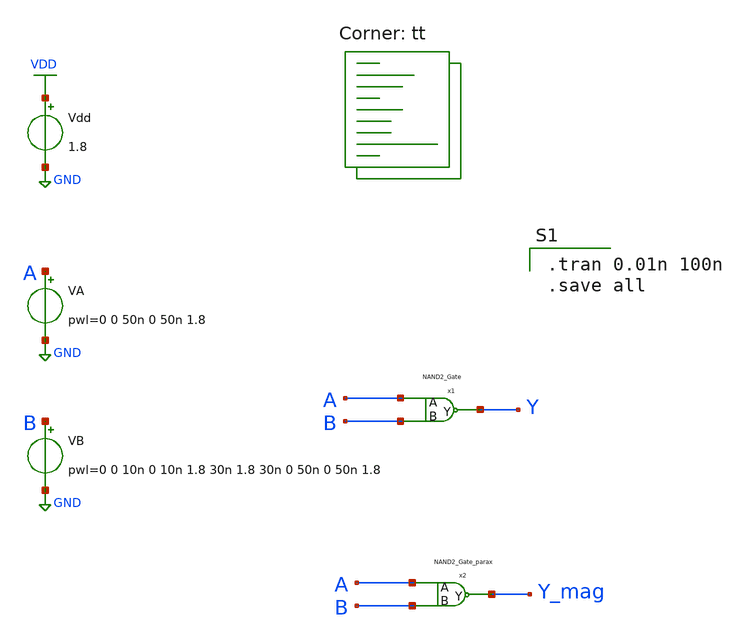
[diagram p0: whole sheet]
** sch_path: gates/NANN2sim.sch
**.subckt NANN2sim
Vdd VDD GND 1.8
VA A GND pwl=0 0 50n 0 50n 1.8
VB B GND pwl=0 0 10n 0 10n 1.8 30n 1.8 30n 0 50n 0 50n 1.8
x1 A Y B NAND2_Gate
x2 A Y_mag B NAND2_Gate_parax
**** begin user architecture code

.tran 0.01n 100n
.save all

.lib $::SKYWATER_MODELS/sky130.lib.spice tt
**** end user architecture code
**.ends

* expanding   symbol:  NAND2_Gate.sym # of pins=3
** sym_path: gates/NAND2_Gate.sym
** sch_path: gates/NAND2_Gate.sch
.subckt NAND2_Gate A Y B
*.ipin A
*.ipin B
*.opin Y
XM1 Y A net1 GND sky130_fd_pr__nfet_01v8 L=0.15 W=1 nf=1 ad='int((nf+1)/2) * W/nf * 0.29' as='int((nf+2)/2) * W/nf * 0.29'
+ pd='2*int((nf+1)/2) * (W/nf + 0.29)' ps='2*int((nf+2)/2) * (W/nf + 0.29)' nrd='0.29 / W' nrs='0.29 / W'
+ sa=0 sb=0 sd=0 mult=1 m=1
XM2 net1 B GND GND sky130_fd_pr__nfet_01v8 L=0.15 W=1 nf=1 ad='int((nf+1)/2) * W/nf * 0.29' as='int((nf+2)/2) * W/nf * 0.29'
+ pd='2*int((nf+1)/2) * (W/nf + 0.29)' ps='2*int((nf+2)/2) * (W/nf + 0.29)' nrd='0.29 / W' nrs='0.29 / W'
+ sa=0 sb=0 sd=0 mult=1 m=1
XM3 Y A VDD VDD sky130_fd_pr__pfet_01v8 L=0.15 W=1 nf=1 ad='int((nf+1)/2) * W/nf * 0.29' as='int((nf+2)/2) * W/nf * 0.29'
+ pd='2*int((nf+1)/2) * (W/nf + 0.29)' ps='2*int((nf+2)/2) * (W/nf + 0.29)' nrd='0.29 / W' nrs='0.29 / W'
+ sa=0 sb=0 sd=0 mult=1 m=1
XM4 Y B VDD VDD sky130_fd_pr__pfet_01v8 L=0.15 W=1 nf=1 ad='int((nf+1)/2) * W/nf * 0.29' as='int((nf+2)/2) * W/nf * 0.29'
+ pd='2*int((nf+1)/2) * (W/nf + 0.29)' ps='2*int((nf+2)/2) * (W/nf + 0.29)' nrd='0.29 / W' nrs='0.29 / W'
+ sa=0 sb=0 sd=0 mult=1 m=1
.ends


* expanding   symbol:  NAND2_Gate_parax.sym # of pins=3
** sym_path: gates/NAND2_Gate.sym
.include [file normalize /home/apn/mag_gates/NAND2_Gate_parax.spice]
.GLOBAL VDD
.GLOBAL GND
.end
